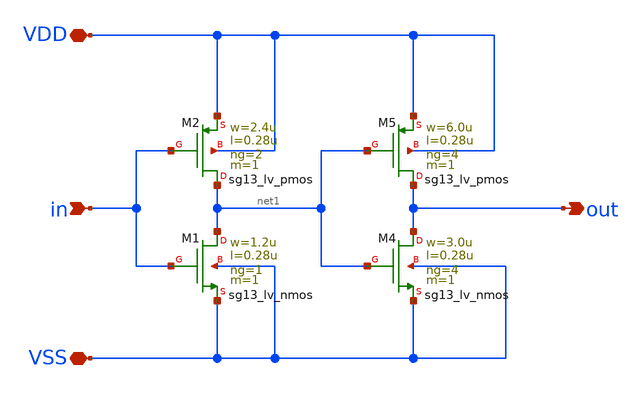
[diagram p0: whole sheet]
** sch_path: blocks/composite/dpi_adexp_neuron/design_data/xschem/buff.sch
**.subckt buff VDD in VSS out
*.iopin VDD
*.ipin in
*.iopin VSS
*.opin out
XM1 net1 in VSS VSS sg13_lv_nmos w=1.2u l=0.28u ng=1 m=1 mm_ok=1
XM2 net1 in VDD VDD sg13_lv_pmos w=2.4u l=0.28u ng=2 m=1 mm_ok=1
XM4 out net1 VSS VSS sg13_lv_nmos w=3.0u l=0.28u ng=4 m=1 mm_ok=1
XM5 out net1 VDD VDD sg13_lv_pmos w=6.0u l=0.28u ng=4 m=1 mm_ok=1
**.ends
.end
